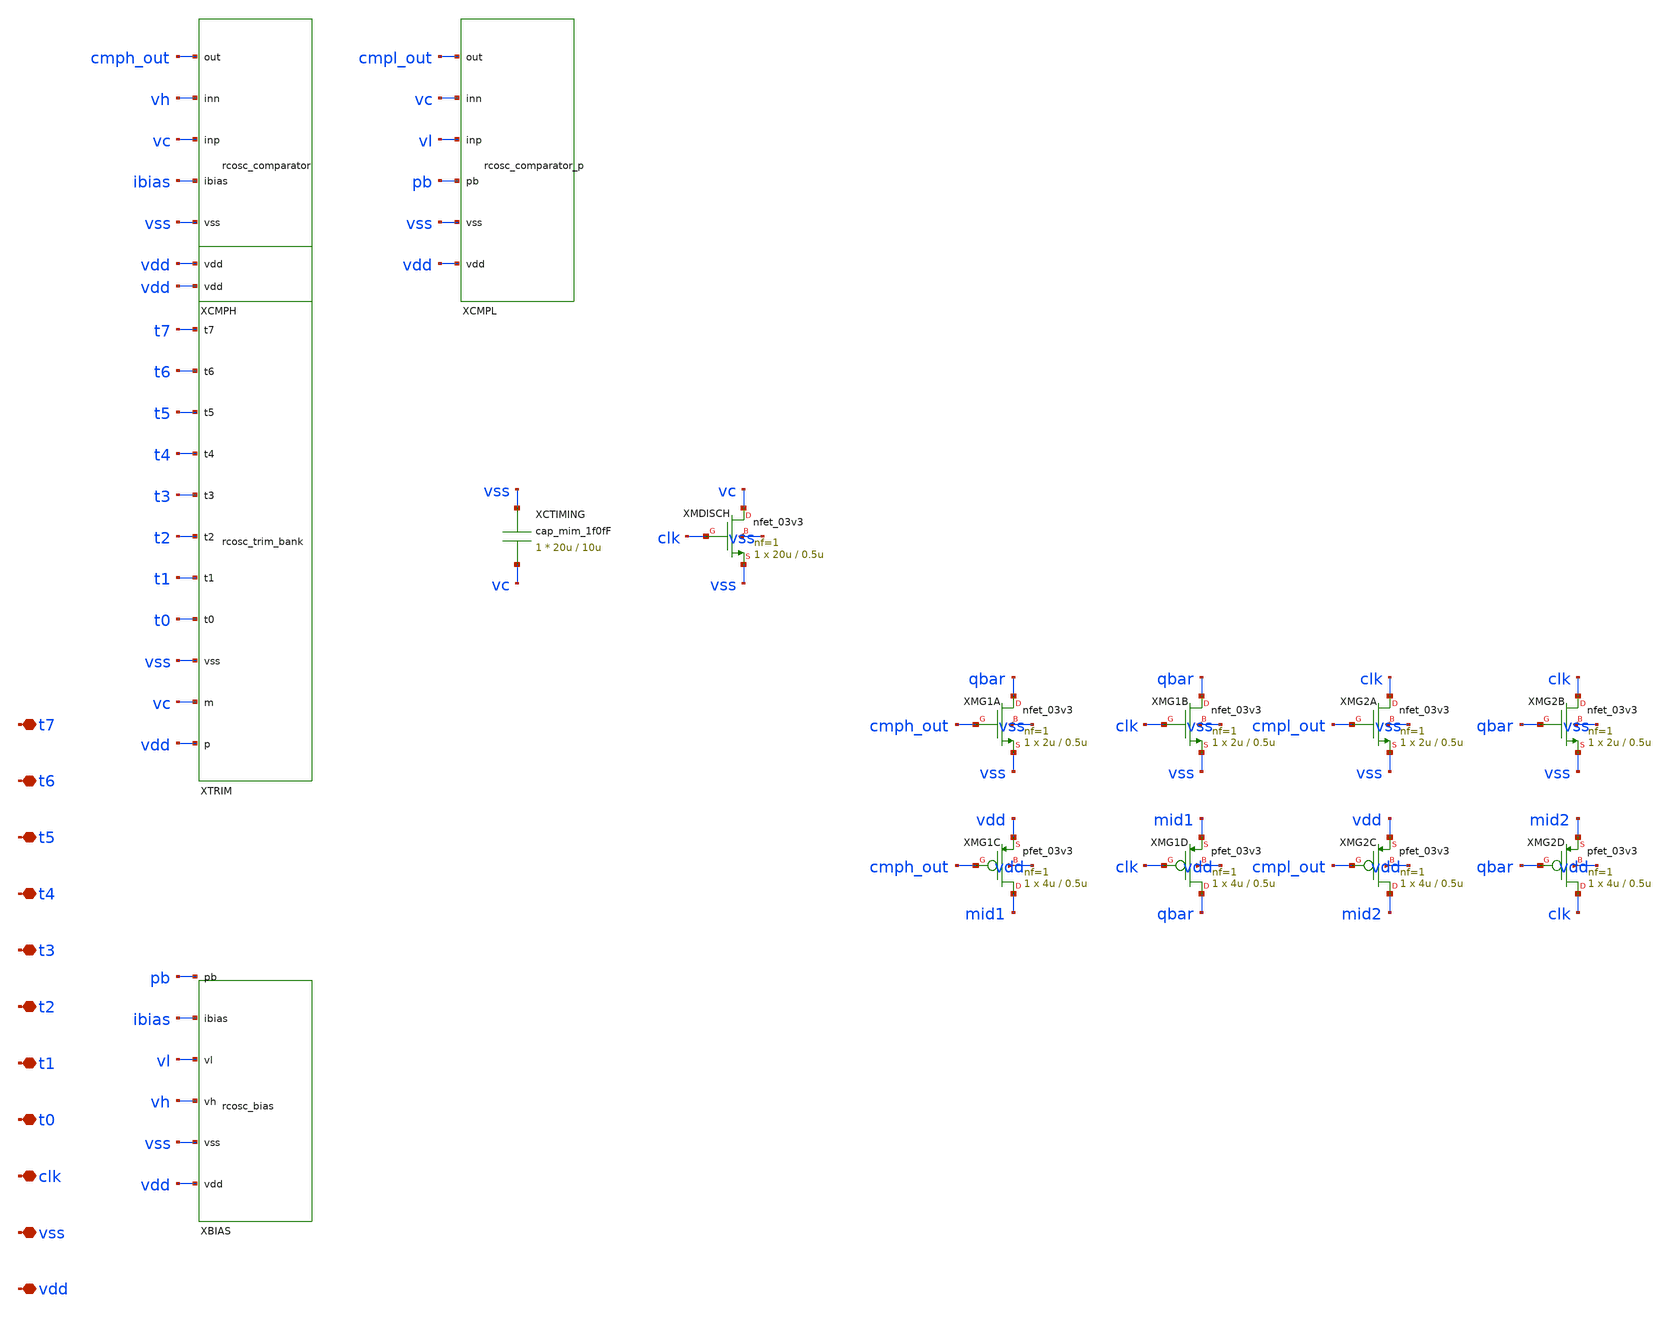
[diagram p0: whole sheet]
** sch_path: design/rcosc_top.sch
**.subckt rcosc_top vdd vss clk t0 t1 t2 t3 t4 t5 t6 t7
*.iopin vdd
*.iopin vss
*.iopin clk
*.iopin t0
*.iopin t1
*.iopin t2
*.iopin t3
*.iopin t4
*.iopin t5
*.iopin t6
*.iopin t7
XXBIAS vdd vss vh vl ibias pb rcosc_bias
XXTRIM vdd vc vss t0 t1 t2 t3 t4 t5 t6 t7 vdd rcosc_trim_bank
XCTIMING vss vc cap_mim_1f0fF c_width=20u c_length=10u m=1
XXCMPH vdd vss ibias vc vh cmph_out rcosc_comparator
XXCMPL vdd vss pb vl vc cmpl_out rcosc_comparator_p
XMDISCH vc clk vss vss nfet_03v3 L=0.5u W=20u nf=1 ad='int((nf+1)/2) * W/nf * 0.18u' as='int((nf+2)/2) * W/nf * 0.18u'
+ pd='2*int((nf+1)/2) * (W/nf + 0.18u)' ps='2*int((nf+2)/2) * (W/nf + 0.18u)' nrd='0.18u / W' nrs='0.18u / W'
+ sa=0 sb=0 sd=0 m=1
XMG1A qbar cmph_out vss vss nfet_03v3 L=0.5u W=2u nf=1 ad='int((nf+1)/2) * W/nf * 0.18u' as='int((nf+2)/2) * W/nf * 0.18u'
+ pd='2*int((nf+1)/2) * (W/nf + 0.18u)' ps='2*int((nf+2)/2) * (W/nf + 0.18u)' nrd='0.18u / W' nrs='0.18u / W'
+ sa=0 sb=0 sd=0 m=1
XMG1B qbar clk vss vss nfet_03v3 L=0.5u W=2u nf=1 ad='int((nf+1)/2) * W/nf * 0.18u' as='int((nf+2)/2) * W/nf * 0.18u'
+ pd='2*int((nf+1)/2) * (W/nf + 0.18u)' ps='2*int((nf+2)/2) * (W/nf + 0.18u)' nrd='0.18u / W' nrs='0.18u / W'
+ sa=0 sb=0 sd=0 m=1
XMG1C mid1 cmph_out vdd vdd pfet_03v3 L=0.5u W=4u nf=1 ad='int((nf+1)/2) * W/nf * 0.18u' as='int((nf+2)/2) * W/nf * 0.18u'
+ pd='2*int((nf+1)/2) * (W/nf + 0.18u)' ps='2*int((nf+2)/2) * (W/nf + 0.18u)' nrd='0.18u / W' nrs='0.18u / W'
+ sa=0 sb=0 sd=0 m=1
XMG1D qbar clk mid1 vdd pfet_03v3 L=0.5u W=4u nf=1 ad='int((nf+1)/2) * W/nf * 0.18u' as='int((nf+2)/2) * W/nf * 0.18u'
+ pd='2*int((nf+1)/2) * (W/nf + 0.18u)' ps='2*int((nf+2)/2) * (W/nf + 0.18u)' nrd='0.18u / W' nrs='0.18u / W'
+ sa=0 sb=0 sd=0 m=1
XMG2A clk cmpl_out vss vss nfet_03v3 L=0.5u W=2u nf=1 ad='int((nf+1)/2) * W/nf * 0.18u' as='int((nf+2)/2) * W/nf * 0.18u'
+ pd='2*int((nf+1)/2) * (W/nf + 0.18u)' ps='2*int((nf+2)/2) * (W/nf + 0.18u)' nrd='0.18u / W' nrs='0.18u / W'
+ sa=0 sb=0 sd=0 m=1
XMG2B clk qbar vss vss nfet_03v3 L=0.5u W=2u nf=1 ad='int((nf+1)/2) * W/nf * 0.18u' as='int((nf+2)/2) * W/nf * 0.18u'
+ pd='2*int((nf+1)/2) * (W/nf + 0.18u)' ps='2*int((nf+2)/2) * (W/nf + 0.18u)' nrd='0.18u / W' nrs='0.18u / W'
+ sa=0 sb=0 sd=0 m=1
XMG2C mid2 cmpl_out vdd vdd pfet_03v3 L=0.5u W=4u nf=1 ad='int((nf+1)/2) * W/nf * 0.18u' as='int((nf+2)/2) * W/nf * 0.18u'
+ pd='2*int((nf+1)/2) * (W/nf + 0.18u)' ps='2*int((nf+2)/2) * (W/nf + 0.18u)' nrd='0.18u / W' nrs='0.18u / W'
+ sa=0 sb=0 sd=0 m=1
XMG2D clk qbar mid2 vdd pfet_03v3 L=0.5u W=4u nf=1 ad='int((nf+1)/2) * W/nf * 0.18u' as='int((nf+2)/2) * W/nf * 0.18u'
+ pd='2*int((nf+1)/2) * (W/nf + 0.18u)' ps='2*int((nf+2)/2) * (W/nf + 0.18u)' nrd='0.18u / W' nrs='0.18u / W'
+ sa=0 sb=0 sd=0 m=1
**.ends

* expanding   symbol:  rcosc_bias.sym # of pins=6
** sym_path: design/rcosc_bias.sym
** sch_path: design/rcosc_bias.sch
.subckt rcosc_bias vdd vss vh vl ibias pb

*.iopin vdd
*.iopin vss
*.iopin vh
*.iopin vl
*.iopin ibias
*.iopin pb
XRBA vdd vh vss ppolyf_u_1k r_width=2u r_length=100u m=1
XRBB vh vl vss ppolyf_u_1k r_width=2u r_length=100u m=1
XRBC vl vss vss ppolyf_u_1k r_width=2u r_length=100u m=1
XN1 ibias ibias vss vss nfet_03v3 L=1u W=2u nf=1 ad='int((nf+1)/2) * W/nf * 0.18u' as='int((nf+2)/2) * W/nf * 0.18u'
+ pd='2*int((nf+1)/2) * (W/nf + 0.18u)' ps='2*int((nf+2)/2) * (W/nf + 0.18u)' nrd='0.18u / W' nrs='0.18u / W'
+ sa=0 sb=0 sd=0 m=1
XN2 pb ibias n2s vss nfet_03v3 L=1u W=16u nf=8 ad='int((nf+1)/2) * W/nf * 0.18u' as='int((nf+2)/2) * W/nf * 0.18u'
+ pd='2*int((nf+1)/2) * (W/nf + 0.18u)' ps='2*int((nf+2)/2) * (W/nf + 0.18u)' nrd='0.18u / W' nrs='0.18u / W'
+ sa=0 sb=0 sd=0 m=1
XRZ n2s vss vss ppolyf_u_1k r_width=2u r_length=32u m=1
XP1 pb pb vdd vdd pfet_03v3 L=1u W=4u nf=1 ad='int((nf+1)/2) * W/nf * 0.18u' as='int((nf+2)/2) * W/nf * 0.18u'
+ pd='2*int((nf+1)/2) * (W/nf + 0.18u)' ps='2*int((nf+2)/2) * (W/nf + 0.18u)' nrd='0.18u / W' nrs='0.18u / W'
+ sa=0 sb=0 sd=0 m=1
XP2 ibias pb vdd vdd pfet_03v3 L=1u W=4u nf=1 ad='int((nf+1)/2) * W/nf * 0.18u' as='int((nf+2)/2) * W/nf * 0.18u'
+ pd='2*int((nf+1)/2) * (W/nf + 0.18u)' ps='2*int((nf+2)/2) * (W/nf + 0.18u)' nrd='0.18u / W' nrs='0.18u / W'
+ sa=0 sb=0 sd=0 m=1
XSEED pb vl vss vss nfet_03v3 L=20u W=2u nf=1 ad='int((nf+1)/2) * W/nf * 0.18u' as='int((nf+2)/2) * W/nf * 0.18u'
+ pd='2*int((nf+1)/2) * (W/nf + 0.18u)' ps='2*int((nf+2)/2) * (W/nf + 0.18u)' nrd='0.18u / W' nrs='0.18u / W'
+ sa=0 sb=0 sd=0 m=1
.ends


* expanding   symbol:  rcosc_trim_bank.sym # of pins=12
** sym_path: design/rcosc_trim_bank.sym
** sch_path: design/rcosc_trim_bank.sch
.subckt rcosc_trim_bank p m vss t0 t1 t2 t3 t4 t5 t6 t7 vdd

*.iopin p
*.iopin m
*.iopin vss
*.iopin t0
*.iopin t1
*.iopin t2
*.iopin t3
*.iopin t4
*.iopin t5
*.iopin t6
*.iopin t7
*.iopin vdd
XRFIX p c1 vss ppolyf_u_1k r_width=2u r_length=17.198u m=1
XR0 c1 c2 vss ppolyf_u_1k r_width=2u r_length=0.7482u m=1
XSW0 c1 t0 c2 vss nfet_03v3 L=0.28u W=24uu nf=1 ad='int((nf+1)/2) * W/nf * 0.18u' as='int((nf+2)/2) * W/nf * 0.18u'
+ pd='2*int((nf+1)/2) * (W/nf + 0.18u)' ps='2*int((nf+2)/2) * (W/nf + 0.18u)' nrd='0.18u / W' nrs='0.18u / W'
+ sa=0 sb=0 sd=0 m=1
XPW0 c2 tb0 c1 vdd pfet_03v3 L=0.28u W=24uu nf=1 ad='int((nf+1)/2) * W/nf * 0.18u' as='int((nf+2)/2) * W/nf * 0.18u'
+ pd='2*int((nf+1)/2) * (W/nf + 0.18u)' ps='2*int((nf+2)/2) * (W/nf + 0.18u)' nrd='0.18u / W' nrs='0.18u / W'
+ sa=0 sb=0 sd=0 m=1
XNINV0 tb0 t0 vss vss nfet_03v3 L=0.5u W=2u nf=1 ad='int((nf+1)/2) * W/nf * 0.18u' as='int((nf+2)/2) * W/nf * 0.18u'
+ pd='2*int((nf+1)/2) * (W/nf + 0.18u)' ps='2*int((nf+2)/2) * (W/nf + 0.18u)' nrd='0.18u / W' nrs='0.18u / W'
+ sa=0 sb=0 sd=0 m=1
XPINV0 tb0 t0 vdd vdd pfet_03v3 L=0.5u W=4u nf=1 ad='int((nf+1)/2) * W/nf * 0.18u' as='int((nf+2)/2) * W/nf * 0.18u'
+ pd='2*int((nf+1)/2) * (W/nf + 0.18u)' ps='2*int((nf+2)/2) * (W/nf + 0.18u)' nrd='0.18u / W' nrs='0.18u / W'
+ sa=0 sb=0 sd=0 m=1
XR1 c2 c3 vss ppolyf_u_1k r_width=2u r_length=1.4965u m=1
XSW1 c2 t1 c3 vss nfet_03v3 L=0.28u W=16uu nf=1 ad='int((nf+1)/2) * W/nf * 0.18u' as='int((nf+2)/2) * W/nf * 0.18u'
+ pd='2*int((nf+1)/2) * (W/nf + 0.18u)' ps='2*int((nf+2)/2) * (W/nf + 0.18u)' nrd='0.18u / W' nrs='0.18u / W'
+ sa=0 sb=0 sd=0 m=1
XPW1 c3 tb1 c2 vdd pfet_03v3 L=0.28u W=16uu nf=1 ad='int((nf+1)/2) * W/nf * 0.18u' as='int((nf+2)/2) * W/nf * 0.18u'
+ pd='2*int((nf+1)/2) * (W/nf + 0.18u)' ps='2*int((nf+2)/2) * (W/nf + 0.18u)' nrd='0.18u / W' nrs='0.18u / W'
+ sa=0 sb=0 sd=0 m=1
XNINV1 tb1 t1 vss vss nfet_03v3 L=0.5u W=2u nf=1 ad='int((nf+1)/2) * W/nf * 0.18u' as='int((nf+2)/2) * W/nf * 0.18u'
+ pd='2*int((nf+1)/2) * (W/nf + 0.18u)' ps='2*int((nf+2)/2) * (W/nf + 0.18u)' nrd='0.18u / W' nrs='0.18u / W'
+ sa=0 sb=0 sd=0 m=1
XPINV1 tb1 t1 vdd vdd pfet_03v3 L=0.5u W=4u nf=1 ad='int((nf+1)/2) * W/nf * 0.18u' as='int((nf+2)/2) * W/nf * 0.18u'
+ pd='2*int((nf+1)/2) * (W/nf + 0.18u)' ps='2*int((nf+2)/2) * (W/nf + 0.18u)' nrd='0.18u / W' nrs='0.18u / W'
+ sa=0 sb=0 sd=0 m=1
XR2 c3 c4 vss ppolyf_u_1k r_width=2u r_length=2.993u m=1
XSW2 c3 t2 c4 vss nfet_03v3 L=0.28u W=12uu nf=1 ad='int((nf+1)/2) * W/nf * 0.18u' as='int((nf+2)/2) * W/nf * 0.18u'
+ pd='2*int((nf+1)/2) * (W/nf + 0.18u)' ps='2*int((nf+2)/2) * (W/nf + 0.18u)' nrd='0.18u / W' nrs='0.18u / W'
+ sa=0 sb=0 sd=0 m=1
XPW2 c4 tb2 c3 vdd pfet_03v3 L=0.28u W=12uu nf=1 ad='int((nf+1)/2) * W/nf * 0.18u' as='int((nf+2)/2) * W/nf * 0.18u'
+ pd='2*int((nf+1)/2) * (W/nf + 0.18u)' ps='2*int((nf+2)/2) * (W/nf + 0.18u)' nrd='0.18u / W' nrs='0.18u / W'
+ sa=0 sb=0 sd=0 m=1
XNINV2 tb2 t2 vss vss nfet_03v3 L=0.5u W=2u nf=1 ad='int((nf+1)/2) * W/nf * 0.18u' as='int((nf+2)/2) * W/nf * 0.18u'
+ pd='2*int((nf+1)/2) * (W/nf + 0.18u)' ps='2*int((nf+2)/2) * (W/nf + 0.18u)' nrd='0.18u / W' nrs='0.18u / W'
+ sa=0 sb=0 sd=0 m=1
XPINV2 tb2 t2 vdd vdd pfet_03v3 L=0.5u W=4u nf=1 ad='int((nf+1)/2) * W/nf * 0.18u' as='int((nf+2)/2) * W/nf * 0.18u'
+ pd='2*int((nf+1)/2) * (W/nf + 0.18u)' ps='2*int((nf+2)/2) * (W/nf + 0.18u)' nrd='0.18u / W' nrs='0.18u / W'
+ sa=0 sb=0 sd=0 m=1
XR3 c4 c5 vss ppolyf_u_1k r_width=2u r_length=5.9859u m=1
XSW3 c4 t3 c5 vss nfet_03v3 L=0.28u W=8uu nf=1 ad='int((nf+1)/2) * W/nf * 0.18u' as='int((nf+2)/2) * W/nf * 0.18u'
+ pd='2*int((nf+1)/2) * (W/nf + 0.18u)' ps='2*int((nf+2)/2) * (W/nf + 0.18u)' nrd='0.18u / W' nrs='0.18u / W'
+ sa=0 sb=0 sd=0 m=1
XPW3 c5 tb3 c4 vdd pfet_03v3 L=0.28u W=8uu nf=1 ad='int((nf+1)/2) * W/nf * 0.18u' as='int((nf+2)/2) * W/nf * 0.18u'
+ pd='2*int((nf+1)/2) * (W/nf + 0.18u)' ps='2*int((nf+2)/2) * (W/nf + 0.18u)' nrd='0.18u / W' nrs='0.18u / W'
+ sa=0 sb=0 sd=0 m=1
XNINV3 tb3 t3 vss vss nfet_03v3 L=0.5u W=2u nf=1 ad='int((nf+1)/2) * W/nf * 0.18u' as='int((nf+2)/2) * W/nf * 0.18u'
+ pd='2*int((nf+1)/2) * (W/nf + 0.18u)' ps='2*int((nf+2)/2) * (W/nf + 0.18u)' nrd='0.18u / W' nrs='0.18u / W'
+ sa=0 sb=0 sd=0 m=1
XPINV3 tb3 t3 vdd vdd pfet_03v3 L=0.5u W=4u nf=1 ad='int((nf+1)/2) * W/nf * 0.18u' as='int((nf+2)/2) * W/nf * 0.18u'
+ pd='2*int((nf+1)/2) * (W/nf + 0.18u)' ps='2*int((nf+2)/2) * (W/nf + 0.18u)' nrd='0.18u / W' nrs='0.18u / W'
+ sa=0 sb=0 sd=0 m=1
XR4 c5 c6 vss ppolyf_u_1k r_width=2u r_length=11.9719u m=1
XSW4 c5 t4 c6 vss nfet_03v3 L=0.28u W=6uu nf=1 ad='int((nf+1)/2) * W/nf * 0.18u' as='int((nf+2)/2) * W/nf * 0.18u'
+ pd='2*int((nf+1)/2) * (W/nf + 0.18u)' ps='2*int((nf+2)/2) * (W/nf + 0.18u)' nrd='0.18u / W' nrs='0.18u / W'
+ sa=0 sb=0 sd=0 m=1
XPW4 c6 tb4 c5 vdd pfet_03v3 L=0.28u W=6uu nf=1 ad='int((nf+1)/2) * W/nf * 0.18u' as='int((nf+2)/2) * W/nf * 0.18u'
+ pd='2*int((nf+1)/2) * (W/nf + 0.18u)' ps='2*int((nf+2)/2) * (W/nf + 0.18u)' nrd='0.18u / W' nrs='0.18u / W'
+ sa=0 sb=0 sd=0 m=1
XNINV4 tb4 t4 vss vss nfet_03v3 L=0.5u W=2u nf=1 ad='int((nf+1)/2) * W/nf * 0.18u' as='int((nf+2)/2) * W/nf * 0.18u'
+ pd='2*int((nf+1)/2) * (W/nf + 0.18u)' ps='2*int((nf+2)/2) * (W/nf + 0.18u)' nrd='0.18u / W' nrs='0.18u / W'
+ sa=0 sb=0 sd=0 m=1
XPINV4 tb4 t4 vdd vdd pfet_03v3 L=0.5u W=4u nf=1 ad='int((nf+1)/2) * W/nf * 0.18u' as='int((nf+2)/2) * W/nf * 0.18u'
+ pd='2*int((nf+1)/2) * (W/nf + 0.18u)' ps='2*int((nf+2)/2) * (W/nf + 0.18u)' nrd='0.18u / W' nrs='0.18u / W'
+ sa=0 sb=0 sd=0 m=1
XR5 c6 c7 vss ppolyf_u_1k r_width=2u r_length=23.9438u m=1
XSW5 c6 t5 c7 vss nfet_03v3 L=0.28u W=5uu nf=1 ad='int((nf+1)/2) * W/nf * 0.18u' as='int((nf+2)/2) * W/nf * 0.18u'
+ pd='2*int((nf+1)/2) * (W/nf + 0.18u)' ps='2*int((nf+2)/2) * (W/nf + 0.18u)' nrd='0.18u / W' nrs='0.18u / W'
+ sa=0 sb=0 sd=0 m=1
XPW5 c7 tb5 c6 vdd pfet_03v3 L=0.28u W=5uu nf=1 ad='int((nf+1)/2) * W/nf * 0.18u' as='int((nf+2)/2) * W/nf * 0.18u'
+ pd='2*int((nf+1)/2) * (W/nf + 0.18u)' ps='2*int((nf+2)/2) * (W/nf + 0.18u)' nrd='0.18u / W' nrs='0.18u / W'
+ sa=0 sb=0 sd=0 m=1
XNINV5 tb5 t5 vss vss nfet_03v3 L=0.5u W=2u nf=1 ad='int((nf+1)/2) * W/nf * 0.18u' as='int((nf+2)/2) * W/nf * 0.18u'
+ pd='2*int((nf+1)/2) * (W/nf + 0.18u)' ps='2*int((nf+2)/2) * (W/nf + 0.18u)' nrd='0.18u / W' nrs='0.18u / W'
+ sa=0 sb=0 sd=0 m=1
XPINV5 tb5 t5 vdd vdd pfet_03v3 L=0.5u W=4u nf=1 ad='int((nf+1)/2) * W/nf * 0.18u' as='int((nf+2)/2) * W/nf * 0.18u'
+ pd='2*int((nf+1)/2) * (W/nf + 0.18u)' ps='2*int((nf+2)/2) * (W/nf + 0.18u)' nrd='0.18u / W' nrs='0.18u / W'
+ sa=0 sb=0 sd=0 m=1
XR6 c7 c8 vss ppolyf_u_1k r_width=2u r_length=47.8876u m=1
XSW6 c7 t6 c8 vss nfet_03v3 L=0.28u W=4uu nf=1 ad='int((nf+1)/2) * W/nf * 0.18u' as='int((nf+2)/2) * W/nf * 0.18u'
+ pd='2*int((nf+1)/2) * (W/nf + 0.18u)' ps='2*int((nf+2)/2) * (W/nf + 0.18u)' nrd='0.18u / W' nrs='0.18u / W'
+ sa=0 sb=0 sd=0 m=1
XPW6 c8 tb6 c7 vdd pfet_03v3 L=0.28u W=4uu nf=1 ad='int((nf+1)/2) * W/nf * 0.18u' as='int((nf+2)/2) * W/nf * 0.18u'
+ pd='2*int((nf+1)/2) * (W/nf + 0.18u)' ps='2*int((nf+2)/2) * (W/nf + 0.18u)' nrd='0.18u / W' nrs='0.18u / W'
+ sa=0 sb=0 sd=0 m=1
XNINV6 tb6 t6 vss vss nfet_03v3 L=0.5u W=2u nf=1 ad='int((nf+1)/2) * W/nf * 0.18u' as='int((nf+2)/2) * W/nf * 0.18u'
+ pd='2*int((nf+1)/2) * (W/nf + 0.18u)' ps='2*int((nf+2)/2) * (W/nf + 0.18u)' nrd='0.18u / W' nrs='0.18u / W'
+ sa=0 sb=0 sd=0 m=1
XPINV6 tb6 t6 vdd vdd pfet_03v3 L=0.5u W=4u nf=1 ad='int((nf+1)/2) * W/nf * 0.18u' as='int((nf+2)/2) * W/nf * 0.18u'
+ pd='2*int((nf+1)/2) * (W/nf + 0.18u)' ps='2*int((nf+2)/2) * (W/nf + 0.18u)' nrd='0.18u / W' nrs='0.18u / W'
+ sa=0 sb=0 sd=0 m=1
XR7 c8 m vss ppolyf_u_1k r_width=2u r_length=95.7751u m=1
XSW7 c8 t7 m vss nfet_03v3 L=0.28u W=3uu nf=1 ad='int((nf+1)/2) * W/nf * 0.18u' as='int((nf+2)/2) * W/nf * 0.18u'
+ pd='2*int((nf+1)/2) * (W/nf + 0.18u)' ps='2*int((nf+2)/2) * (W/nf + 0.18u)' nrd='0.18u / W' nrs='0.18u / W'
+ sa=0 sb=0 sd=0 m=1
XPW7 m tb7 c8 vdd pfet_03v3 L=0.28u W=3uu nf=1 ad='int((nf+1)/2) * W/nf * 0.18u' as='int((nf+2)/2) * W/nf * 0.18u'
+ pd='2*int((nf+1)/2) * (W/nf + 0.18u)' ps='2*int((nf+2)/2) * (W/nf + 0.18u)' nrd='0.18u / W' nrs='0.18u / W'
+ sa=0 sb=0 sd=0 m=1
XNINV7 tb7 t7 vss vss nfet_03v3 L=0.5u W=2u nf=1 ad='int((nf+1)/2) * W/nf * 0.18u' as='int((nf+2)/2) * W/nf * 0.18u'
+ pd='2*int((nf+1)/2) * (W/nf + 0.18u)' ps='2*int((nf+2)/2) * (W/nf + 0.18u)' nrd='0.18u / W' nrs='0.18u / W'
+ sa=0 sb=0 sd=0 m=1
XPINV7 tb7 t7 vdd vdd pfet_03v3 L=0.5u W=4u nf=1 ad='int((nf+1)/2) * W/nf * 0.18u' as='int((nf+2)/2) * W/nf * 0.18u'
+ pd='2*int((nf+1)/2) * (W/nf + 0.18u)' ps='2*int((nf+2)/2) * (W/nf + 0.18u)' nrd='0.18u / W' nrs='0.18u / W'
+ sa=0 sb=0 sd=0 m=1
.ends


* expanding   symbol:  rcosc_comparator.sym # of pins=6
** sym_path: design/rcosc_comparator.sym
** sch_path: design/rcosc_comparator.sch
.subckt rcosc_comparator vdd vss ibias inp inn out

*.iopin vdd
*.iopin vss
*.iopin ibias
*.iopin inp
*.iopin inn
*.iopin out
XMTAIL tail ibias vss vss nfet_03v3 L=1u W=16u nf=8 ad='int((nf+1)/2) * W/nf * 0.18u' as='int((nf+2)/2) * W/nf * 0.18u'
+ pd='2*int((nf+1)/2) * (W/nf + 0.18u)' ps='2*int((nf+2)/2) * (W/nf + 0.18u)' nrd='0.18u / W' nrs='0.18u / W'
+ sa=0 sb=0 sd=0 m=1
XMINP dp inp tail vss nfet_03v3 L=0.5u W=4u nf=1 ad='int((nf+1)/2) * W/nf * 0.18u' as='int((nf+2)/2) * W/nf * 0.18u'
+ pd='2*int((nf+1)/2) * (W/nf + 0.18u)' ps='2*int((nf+2)/2) * (W/nf + 0.18u)' nrd='0.18u / W' nrs='0.18u / W'
+ sa=0 sb=0 sd=0 m=1
XMINN dn inn tail vss nfet_03v3 L=0.5u W=4u nf=1 ad='int((nf+1)/2) * W/nf * 0.18u' as='int((nf+2)/2) * W/nf * 0.18u'
+ pd='2*int((nf+1)/2) * (W/nf + 0.18u)' ps='2*int((nf+2)/2) * (W/nf + 0.18u)' nrd='0.18u / W' nrs='0.18u / W'
+ sa=0 sb=0 sd=0 m=1
XMLOADA dn dn vdd vdd pfet_03v3 L=1u W=4u nf=1 ad='int((nf+1)/2) * W/nf * 0.18u' as='int((nf+2)/2) * W/nf * 0.18u'
+ pd='2*int((nf+1)/2) * (W/nf + 0.18u)' ps='2*int((nf+2)/2) * (W/nf + 0.18u)' nrd='0.18u / W' nrs='0.18u / W'
+ sa=0 sb=0 sd=0 m=1
XMLOADB dp dn vdd vdd pfet_03v3 L=1u W=4u nf=1 ad='int((nf+1)/2) * W/nf * 0.18u' as='int((nf+2)/2) * W/nf * 0.18u'
+ pd='2*int((nf+1)/2) * (W/nf + 0.18u)' ps='2*int((nf+2)/2) * (W/nf + 0.18u)' nrd='0.18u / W' nrs='0.18u / W'
+ sa=0 sb=0 sd=0 m=1
XMBUFP out dp vdd vdd pfet_03v3 L=0.5u W=4u nf=1 ad='int((nf+1)/2) * W/nf * 0.18u' as='int((nf+2)/2) * W/nf * 0.18u'
+ pd='2*int((nf+1)/2) * (W/nf + 0.18u)' ps='2*int((nf+2)/2) * (W/nf + 0.18u)' nrd='0.18u / W' nrs='0.18u / W'
+ sa=0 sb=0 sd=0 m=1
XMBUFN out dp vss vss nfet_03v3 L=0.5u W=1u nf=1 ad='int((nf+1)/2) * W/nf * 0.18u' as='int((nf+2)/2) * W/nf * 0.18u'
+ pd='2*int((nf+1)/2) * (W/nf + 0.18u)' ps='2*int((nf+2)/2) * (W/nf + 0.18u)' nrd='0.18u / W' nrs='0.18u / W'
+ sa=0 sb=0 sd=0 m=1
.ends


* expanding   symbol:  rcosc_comparator_p.sym # of pins=6
** sym_path: design/rcosc_comparator_p.sym
** sch_path: design/rcosc_comparator_p.sch
.subckt rcosc_comparator_p vdd vss pb inp inn out

*.iopin vdd
*.iopin vss
*.iopin pb
*.iopin inp
*.iopin inn
*.iopin out
XMPTAIL tailp pb vdd vdd pfet_03v3 L=1u W=16u nf=4 ad='int((nf+1)/2) * W/nf * 0.18u' as='int((nf+2)/2) * W/nf * 0.18u'
+ pd='2*int((nf+1)/2) * (W/nf + 0.18u)' ps='2*int((nf+2)/2) * (W/nf + 0.18u)' nrd='0.18u / W' nrs='0.18u / W'
+ sa=0 sb=0 sd=0 m=1
XMPINP dp inn tailp vdd pfet_03v3 L=0.5u W=8u nf=4 ad='int((nf+1)/2) * W/nf * 0.18u' as='int((nf+2)/2) * W/nf * 0.18u'
+ pd='2*int((nf+1)/2) * (W/nf + 0.18u)' ps='2*int((nf+2)/2) * (W/nf + 0.18u)' nrd='0.18u / W' nrs='0.18u / W'
+ sa=0 sb=0 sd=0 m=1
XMPINN dn inp tailp vdd pfet_03v3 L=0.5u W=8u nf=4 ad='int((nf+1)/2) * W/nf * 0.18u' as='int((nf+2)/2) * W/nf * 0.18u'
+ pd='2*int((nf+1)/2) * (W/nf + 0.18u)' ps='2*int((nf+2)/2) * (W/nf + 0.18u)' nrd='0.18u / W' nrs='0.18u / W'
+ sa=0 sb=0 sd=0 m=1
XMNLOADA dn dn vss vss nfet_03v3 L=1u W=4u nf=1 ad='int((nf+1)/2) * W/nf * 0.18u' as='int((nf+2)/2) * W/nf * 0.18u'
+ pd='2*int((nf+1)/2) * (W/nf + 0.18u)' ps='2*int((nf+2)/2) * (W/nf + 0.18u)' nrd='0.18u / W' nrs='0.18u / W'
+ sa=0 sb=0 sd=0 m=1
XMNLOADB dp dn vss vss nfet_03v3 L=1u W=4u nf=1 ad='int((nf+1)/2) * W/nf * 0.18u' as='int((nf+2)/2) * W/nf * 0.18u'
+ pd='2*int((nf+1)/2) * (W/nf + 0.18u)' ps='2*int((nf+2)/2) * (W/nf + 0.18u)' nrd='0.18u / W' nrs='0.18u / W'
+ sa=0 sb=0 sd=0 m=1
XMBUFP outb dp vdd vdd pfet_03v3 L=0.5u W=4u nf=1 ad='int((nf+1)/2) * W/nf * 0.18u' as='int((nf+2)/2) * W/nf * 0.18u'
+ pd='2*int((nf+1)/2) * (W/nf + 0.18u)' ps='2*int((nf+2)/2) * (W/nf + 0.18u)' nrd='0.18u / W' nrs='0.18u / W'
+ sa=0 sb=0 sd=0 m=1
XMBUFN outb dp vss vss nfet_03v3 L=0.5u W=0.5u nf=1 ad='int((nf+1)/2) * W/nf * 0.18u' as='int((nf+2)/2) * W/nf * 0.18u'
+ pd='2*int((nf+1)/2) * (W/nf + 0.18u)' ps='2*int((nf+2)/2) * (W/nf + 0.18u)' nrd='0.18u / W' nrs='0.18u / W'
+ sa=0 sb=0 sd=0 m=1
XMBUF2P out outb vdd vdd pfet_03v3 L=0.5u W=4u nf=1 ad='int((nf+1)/2) * W/nf * 0.18u' as='int((nf+2)/2) * W/nf * 0.18u'
+ pd='2*int((nf+1)/2) * (W/nf + 0.18u)' ps='2*int((nf+2)/2) * (W/nf + 0.18u)' nrd='0.18u / W' nrs='0.18u / W'
+ sa=0 sb=0 sd=0 m=1
XMBUF2N out outb vss vss nfet_03v3 L=0.5u W=2u nf=1 ad='int((nf+1)/2) * W/nf * 0.18u' as='int((nf+2)/2) * W/nf * 0.18u'
+ pd='2*int((nf+1)/2) * (W/nf + 0.18u)' ps='2*int((nf+2)/2) * (W/nf + 0.18u)' nrd='0.18u / W' nrs='0.18u / W'
+ sa=0 sb=0 sd=0 m=1
.ends

.end
